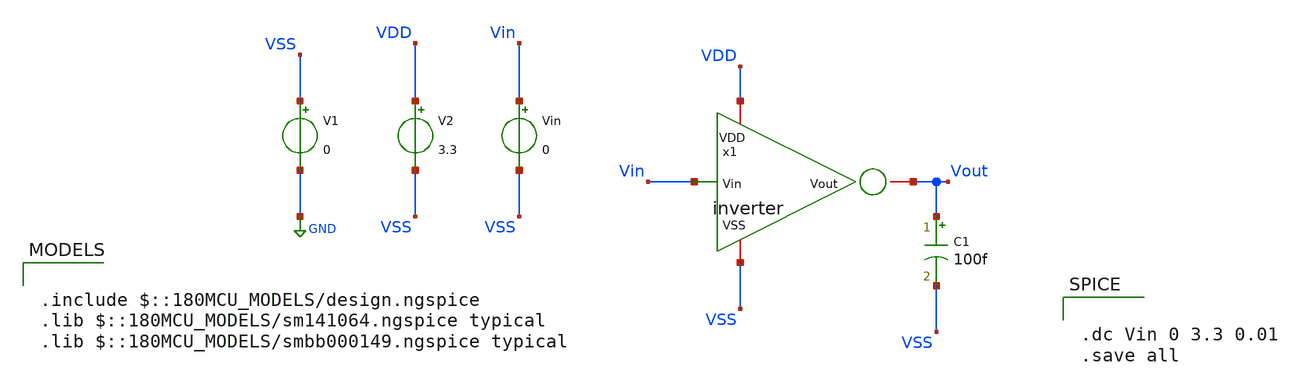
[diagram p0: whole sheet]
** sch_path: gf180_examples/inverter/xschem/inverter_tb_none.sch
**.subckt inverter_tb_none
C1 Vout VSS 100f m=1
V1 VSS GND 0
V2 VDD VSS 3.3
Vin Vin VSS 0
x1 Vin VDD VSS Vout inverter
**** begin user architecture code

.include $::180MCU_MODELS/design.ngspice
.lib $::180MCU_MODELS/sm141064.ngspice typical
.lib $::180MCU_MODELS/smbb000149.ngspice typical



.dc Vin 0 3.3 0.01
.save all


**** end user architecture code
**.ends
.GLOBAL GND
.end
